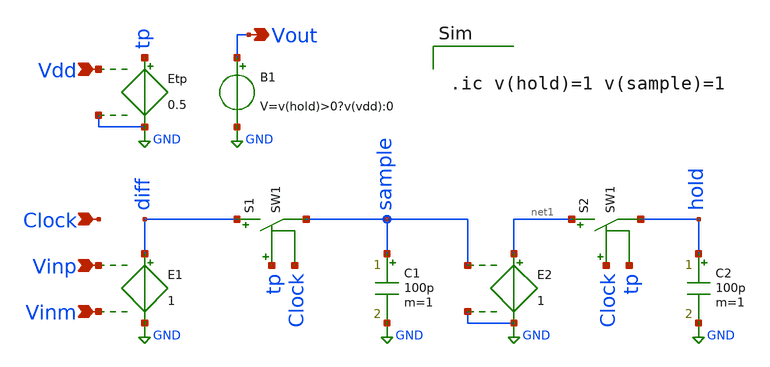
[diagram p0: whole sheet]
** sch_path: real_circuit/final/ideal_comp.sch
**.subckt ideal_comp Vinp Vinm Vdd Clock Vout
*.ipin Vinp
*.ipin Vinm
*.ipin Vdd
*.ipin Clock
*.opin Vout
Etp tp GND Vdd GND 0.5
E1 diff GND Vinp Vinm 1
E2 net1 GND sample GND 1
C1 sample GND 100p m=1
C2 hold GND 100p m=1
S1 diff sample tp Clock SW1
S2 net1 hold Clock tp SW1
B1 Vout GND V=v(hold)>0?v(vdd):0
**** begin user architecture code


.ic v(hold)=1 v(sample)=1


**** end user architecture code
**.ends
.GLOBAL GND
**** begin user architecture code
.MODEL SW1 SW   VT=0.9 VH=0.01  RON=0.01 ROFF=10G
**** end user architecture code
.end
